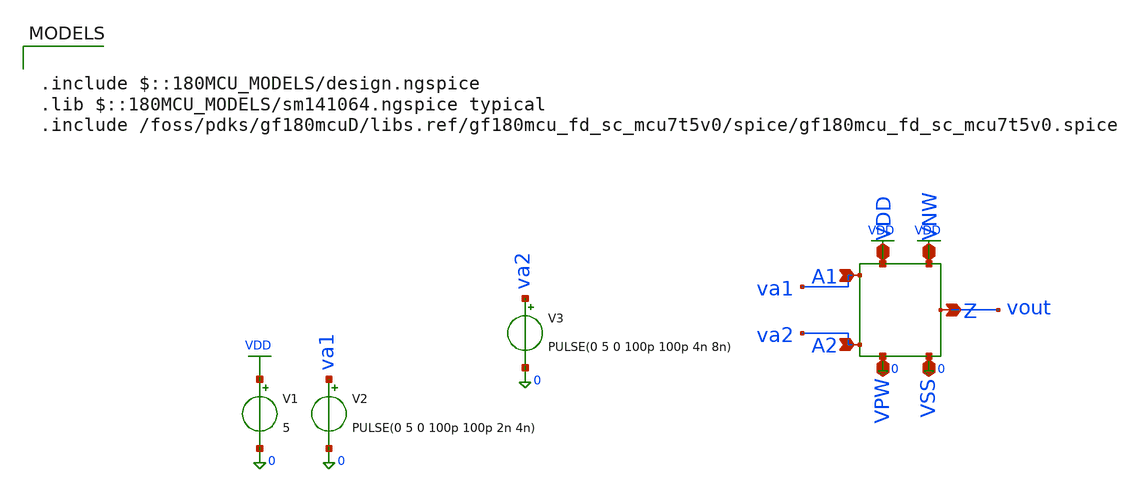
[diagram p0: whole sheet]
** sch_path: src/analog/xor_tb.sch
**.subckt xor_tb
V1 VDD 0 5
V2 va1 0 PULSE(0 5 0 100p 100p 2n 4n)
V3 va2 0 PULSE(0 5 0 100p 100p 4n 8n)
**** begin user architecture code



.control
save all


** Simulations
op
tran 10p 10n

** Plots
setplot tran1

plot v(va1) v(va2) v(vout)

setplot op1
write xor_tb.raw
.endc




.include $::180MCU_MODELS/design.ngspice
.lib $::180MCU_MODELS/sm141064.ngspice typical
.include /foss/pdks/gf180mcuD/libs.ref/gf180mcu_fd_sc_mcu7t5v0/spice/gf180mcu_fd_sc_mcu7t5v0.spice

**** end user architecture code
**.ends
.GLOBAL VDD
.end
